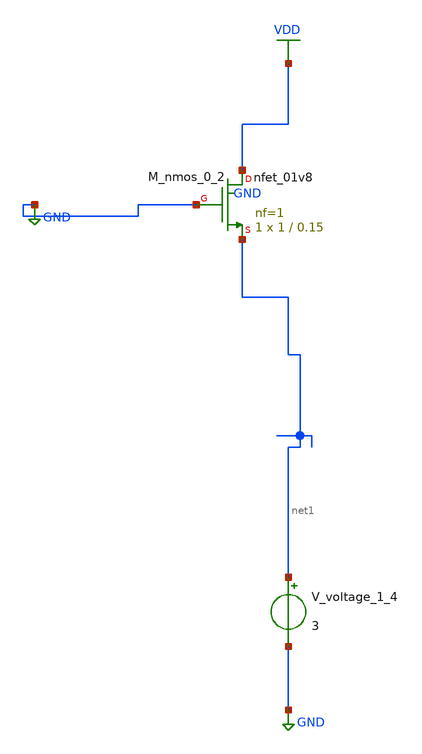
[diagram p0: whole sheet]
** sch_path: schematics/AMSNet/102.sch
**.subckt 102
XM_nmos_0_2 VDD GND net1 GND sky130_fd_pr__nfet_01v8 L=0.15 W=1 nf=1 ad='int((1 + 1)/2) * 1 / 1 * 0.29'
+ as='int((1 + 2)/2) * 1 / 1 * 0.29' pd='2*int((1 + 1)/2) * (1 / 1 + 0.29)' ps='2*int((1 + 2)/2) * (1 / 1 + 0.29)'
+ nrd='0.29 / 1 ' nrs='0.29 / 1 ' sa=0 sb=0 sd=0 mult=1 m=1
V_voltage_1_4 net1 GND 3
**.ends
.GLOBAL GND
.GLOBAL VDD
.end
